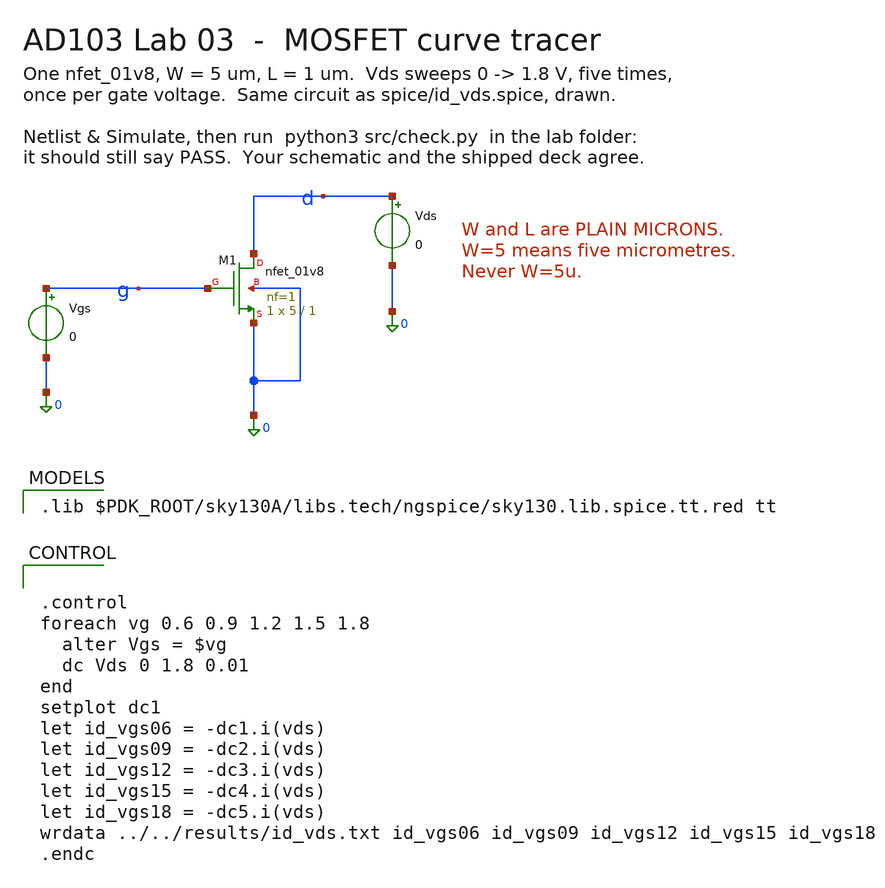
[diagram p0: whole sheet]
** sch_path: labs/lab-03-mosfet-regions/xschem/nmos_curves.sch
**.subckt nmos_curves
XM1 d g 0 0 sky130_fd_pr__nfet_01v8 L=1 W=5 nf=1 ad='int((1 + 1)/2) * 5 / 1 * 0.29' as='int((1 + 2)/2) * 5 / 1 * 0.29'
+ pd='2*int((1 + 1)/2) * (5 / 1 + 0.29)' ps='2*int((1 + 2)/2) * (5 / 1 + 0.29)' nrd='0.29 / 5 ' nrs='0.29 / 5 '
+ sa=0 sb=0 sd=0 mult=1 m=1
Vgs g 0 0
Vds d 0 0
**** begin user architecture code

.lib $PDK_ROOT/sky130A/libs.tech/ngspice/sky130.lib.spice.tt.red tt



.control
foreach vg 0.6 0.9 1.2 1.5 1.8
  alter Vgs = $vg
  dc Vds 0 1.8 0.01
end
setplot dc1
let id_vgs06 = -dc1.i(vds)
let id_vgs09 = -dc2.i(vds)
let id_vgs12 = -dc3.i(vds)
let id_vgs15 = -dc4.i(vds)
let id_vgs18 = -dc5.i(vds)
wrdata ../../results/id_vds.txt id_vgs06 id_vgs09 id_vgs12 id_vgs15 id_vgs18
.endc


**** end user architecture code
**.ends
.end
